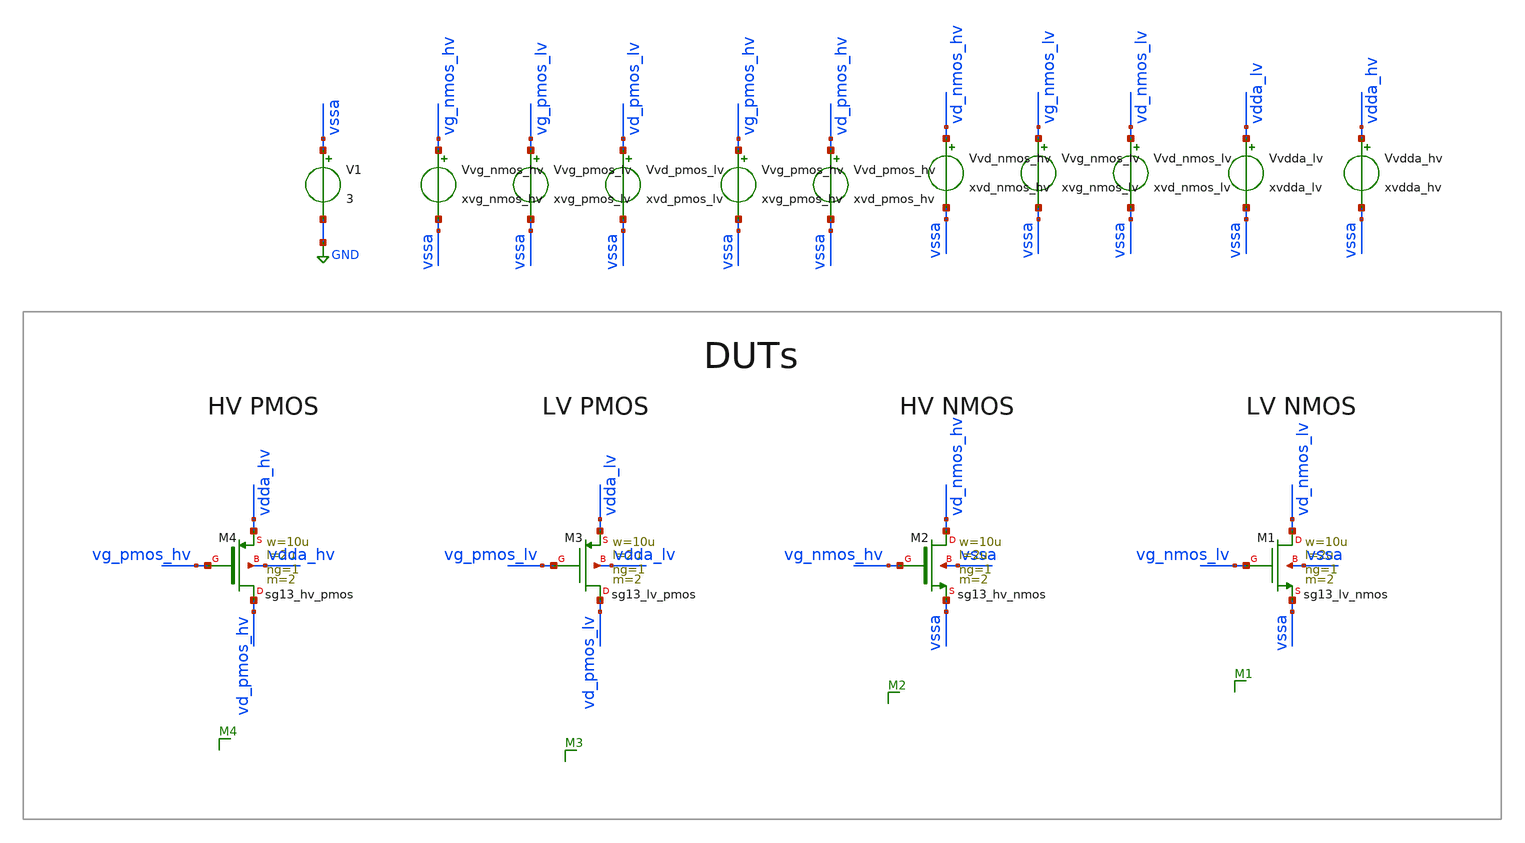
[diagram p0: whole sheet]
** sch_path: tb_vth_ihp/tb_vth_ihp.sch
**.subckt tb_vth_ihp
XM1 vd_nmos_lv vg_nmos_lv vssa vssa sg13_lv_nmos w=10u l=2u ng=1 m=2 mm_ok=1
V1 vssa GND 3
Vvg_nmos_lv vg_nmos_lv vssa xvg_nmos_lv
Vvd_nmos_lv vd_nmos_lv vssa xvd_nmos_lv
XM2 vd_nmos_hv vg_nmos_hv vssa vssa sg13_hv_nmos w=10u l=2u ng=1 m=2 mm_ok=1
Vvdda_lv vdda_lv vssa xvdda_lv
Vvdda_hv vdda_hv vssa xvdda_hv
XM3 vd_pmos_lv vg_pmos_lv vdda_lv vdda_lv sg13_lv_pmos w=10u l=2u ng=1 m=2 mm_ok=1
Vvg_pmos_lv vg_pmos_lv vssa xvg_pmos_lv
Vvd_pmos_lv vd_pmos_lv vssa xvd_pmos_lv
Vvg_pmos_hv vg_pmos_hv vssa xvg_pmos_hv
Vvd_pmos_hv vd_pmos_hv vssa xvd_pmos_hv
XM4 vd_pmos_hv vg_pmos_hv vdda_hv vdda_hv sg13_hv_pmos w=10u l=2u ng=1 m=2 mm_ok=1
Vvg_nmos_hv vg_nmos_hv vssa xvg_nmos_hv
Vvd_nmos_hv vd_nmos_hv vssa xvd_nmos_hv
**** begin user architecture code

** opencircuitdesign pdks install
.lib /home/slice/pdk/iHP/IHP-Open-PDK/ihp-sg13g2/libs.tech/ngspice/models/cornerMOSlv.lib mos_tt
.lib /home/slice/pdk/iHP/IHP-Open-PDK/ihp-sg13g2/libs.tech/ngspice/models/cornerMOShv.lib mos_tt
.lib /home/slice/pdk/iHP/IHP-Open-PDK/ihp-sg13g2/libs.tech/ngspice/models/cornerRES.lib res_typ
.include /home/slice/pdk/iHP/IHP-Open-PDK/ihp-sg13g2/libs.tech/ngspice/models/diodes.lib


* Parameters
.param xvg_nmos_lv = 0.4
.param xvd_nmos_lv = 0.35
.param xvg_nmos_hv = 0.79
.param xvd_nmos_hv = 0.35
.param xvdda_hv = 3.3
.csparam xvdda_hv_var = 'xvdda_hv'
.param xvdda_lv = 1.65
.csparam xvdda_lv_var = 'xvdda_lv'
.param xvg_pmos_lv = 1.1
.param xvg_pmos_hv = 2.414
.param xvd_pmos_lv = 1.3
.param xvd_pmos_hv = 2.95
.param xtsim = 5u
.csparam xtsim_var = 'xtsim'
.param xstep_en = 1
.temp 27


  ** must save the below for DCOP analysis to be back annotated onto the schematic
  .option savecurrents

  .include tb_vth_ihp.save

  *.save all
  .save v(vd_nmos) v(vg_nmos)
  .save @n.xm1.nsg13_lv_nmos[ids] @n.xm2.nsg13_hv_nmos[ids] @n.xm3.nsg13_lv_pmos[ids] @n.xm4.nsg13_hv_pmos[ids]

  .control

    *set xTj = ( -40 -30 -20 -10 0 10 20 30 40 50 60 70 80 90 100 110 120 130 )
    set xTj = ( 27 )
    foreach xTj_var $xTj

    let Tj_meas = $xTj_var

    echo temperature is "$&Tj_meas"

    set temp = $xTj_var


** 1. DCOP ANALYSIS **

  op
  *set filetype=ascii
  remzerovec
  write tb_vth_ihp_op.raw
  echo "$&Tj_meas" >> vth_measures_T.txt
  let vth_meas_nmoslv = @n.xm1.nsg13_lv_nmos[vth]
  echo "$&vth_meas_nmoslv" >> vth_measures_nmoslv_tt.txt
  let vth_meas_nmoshv = @n.xm2.nsg13_hv_nmos[vth]
  echo "$&vth_meas_nmoshv" >> vth_measures_nmoshv_tt.txt
  let vth_meas_pmoslv = @n.xm3.nsg13_lv_pmos[vth]
  echo "$&vth_meas_pmoslv" >> vth_measures_pmoslv_tt.txt
  let vth_meas_pmoshv = @n.xm4.nsg13_hv_pmos[vth]
  echo "$&vth_meas_pmoshv" >> vth_measures_pmoshv_tt.txt

 ** 2. DC ANALYSIS **

  dc Vvd_nmos_lv 0 $&xvdda_lv_var 10m
  remzerovec
  write tb_vth_ihp_nmoslv_dc.raw
  dc Vvd_nmos_hv 0 $&xvdda_hv_var 10m
  remzerovec
  write tb_vth_ihp_nmoshv_dc.raw
  dc Vvd_pmos_lv 0 $&xvdda_lv_var 10m
  remzerovec
  write tb_vth_ihp_pmoslv_dc.raw
  dc Vvd_pmos_hv 0 $&xvdda_hv_var 10m
  remzerovec
  write tb_vth_ihp_pmoshv_dc.raw

  end

  setplot
quit 0
.endc




**** end user architecture code
**.ends
.GLOBAL GND
.end
